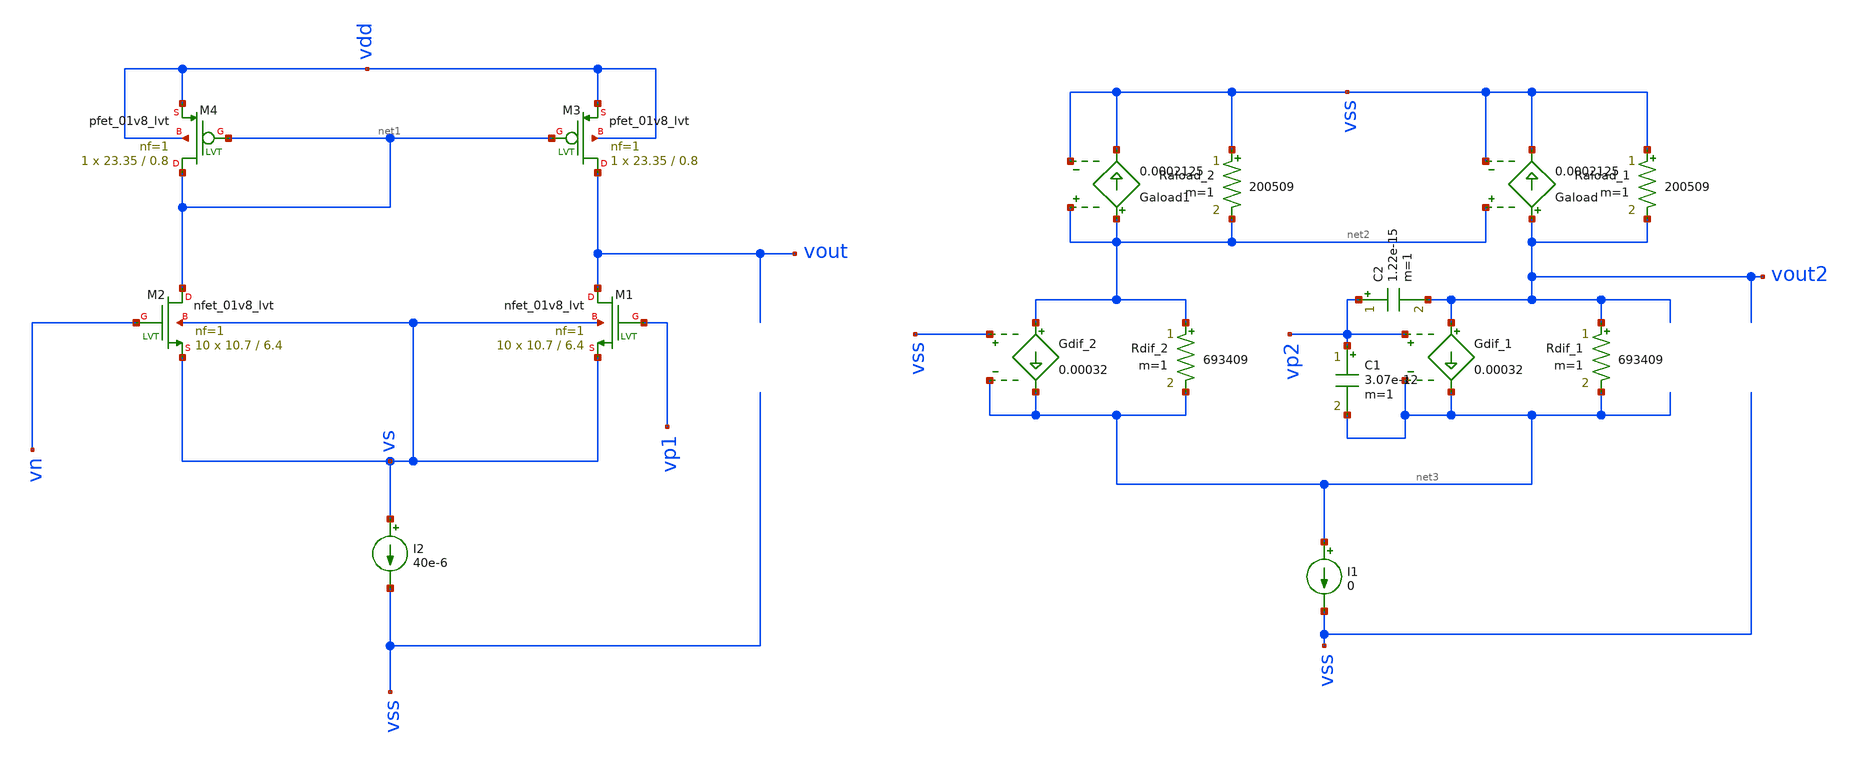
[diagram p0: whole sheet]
** sch_path: test-python/sstadex/xschem/ota_tb_2.sch
**.subckt ota_tb_2
I2 vs vss 40e-6
XM1 vout vp1 vs vs sky130_fd_pr__nfet_01v8_lvt L=6.4 W=10.7 nf=1 ad='int((nf+1)/2) * W/nf * 0.29' as='int((nf+2)/2) * W/nf * 0.29'
+ pd='2*int((nf+1)/2) * (W/nf + 0.29)' ps='2*int((nf+2)/2) * (W/nf + 0.29)' nrd='0.29 / W' nrs='0.29 / W'
+ sa=0 sb=0 sd=0 mult=10 m=10
XM2 net1 vn vs vs sky130_fd_pr__nfet_01v8_lvt L=6.4 W=10.7 nf=1 ad='int((nf+1)/2) * W/nf * 0.29' as='int((nf+2)/2) * W/nf * 0.29'
+ pd='2*int((nf+1)/2) * (W/nf + 0.29)' ps='2*int((nf+2)/2) * (W/nf + 0.29)' nrd='0.29 / W' nrs='0.29 / W'
+ sa=0 sb=0 sd=0 mult=10 m=10
XM3 vout net1 vdd vdd sky130_fd_pr__pfet_01v8_lvt L=0.8 W=23.35 nf=1 ad='int((nf+1)/2) * W/nf * 0.29'
+ as='int((nf+2)/2) * W/nf * 0.29' pd='2*int((nf+1)/2) * (W/nf + 0.29)' ps='2*int((nf+2)/2) * (W/nf + 0.29)'
+ nrd='0.29 / W' nrs='0.29 / W' sa=0 sb=0 sd=0 mult=1 m=1
XM4 net1 net1 vdd vdd sky130_fd_pr__pfet_01v8_lvt L=0.8 W=23.35 nf=1 ad='int((nf+1)/2) * W/nf * 0.29'
+ as='int((nf+2)/2) * W/nf * 0.29' pd='2*int((nf+1)/2) * (W/nf + 0.29)' ps='2*int((nf+2)/2) * (W/nf + 0.29)'
+ nrd='0.29 / W' nrs='0.29 / W' sa=0 sb=0 sd=0 mult=1 m=1
Rdif_2 net2 net3 693409 m=1
Gdif_2 net2 net3 vss net3 0.00032
Rdif_1 vout2 net3 693409 m=1
Gdif_1 vout2 net3 vp2 net3 0.00032
I1 net3 vss 0
Raload_1 vss vout2 200509 m=1
Raload_2 vss net2 200509 m=1
Gaload vout2 vss net2 vss 0.0002125
Gaload1 net2 vss net2 vss 0.0002125
C1 vp2 net3 3.07e-12 m=1
C2 vp2 vout2 1.22e-15 m=1
**** begin user architecture code



.lib /opt/pdks/sky130A/libs.tech/ngspice/sky130.lib.spice tt

Vref vn 0 0.9
Vdd vdd 0 1.8
Vpos vp1 0 0.9 ac 1
Vpos1 vp2 0 0 ac 1
Vss vss 0 0

.control
ac dec 10 1 100G
plot vdb(vout) vdb(vout2)
plot phase(vout)
.endc



**** end user architecture code
**.ends
.end
